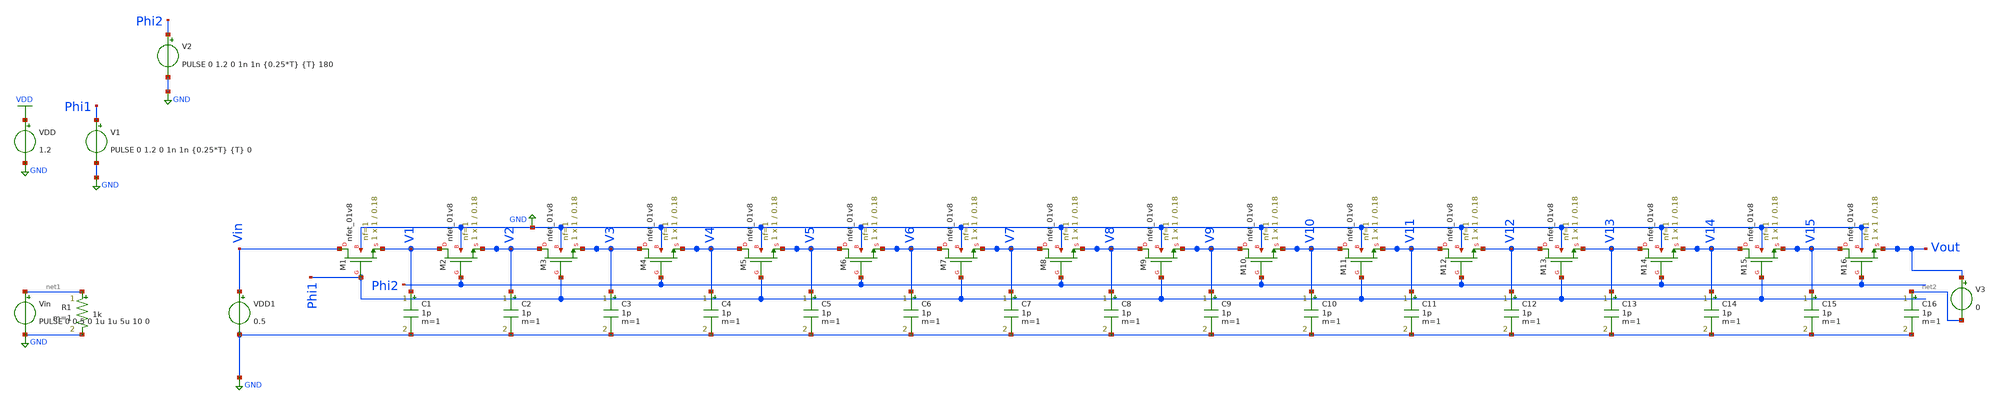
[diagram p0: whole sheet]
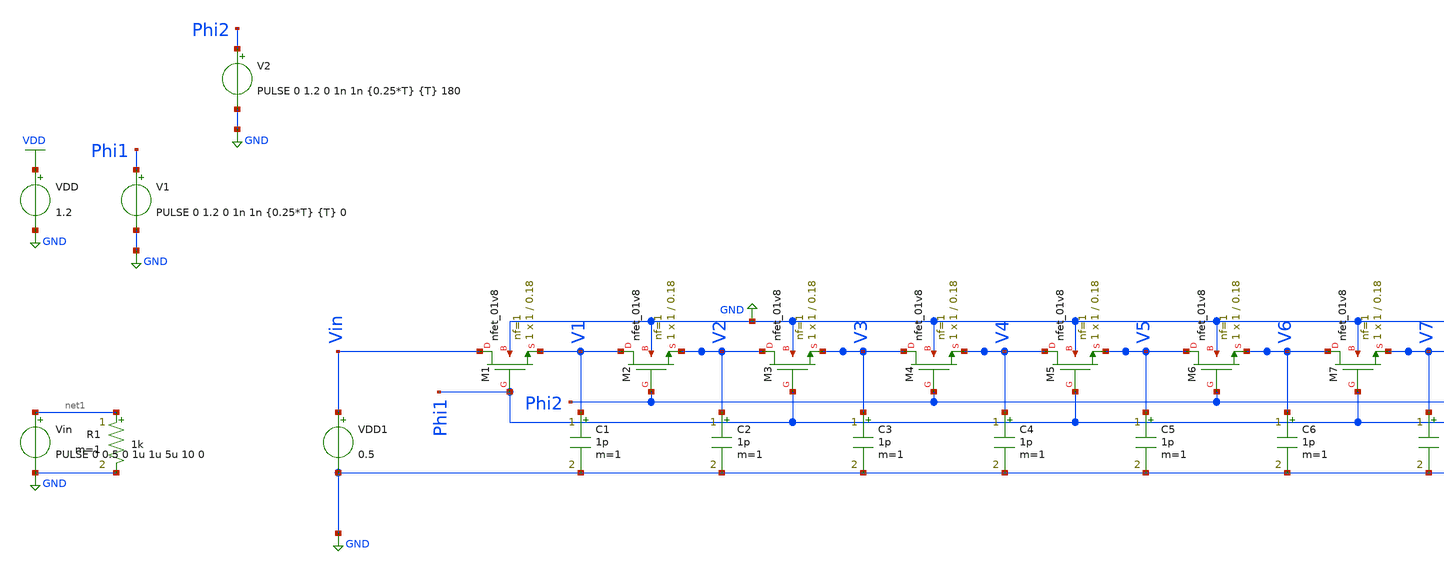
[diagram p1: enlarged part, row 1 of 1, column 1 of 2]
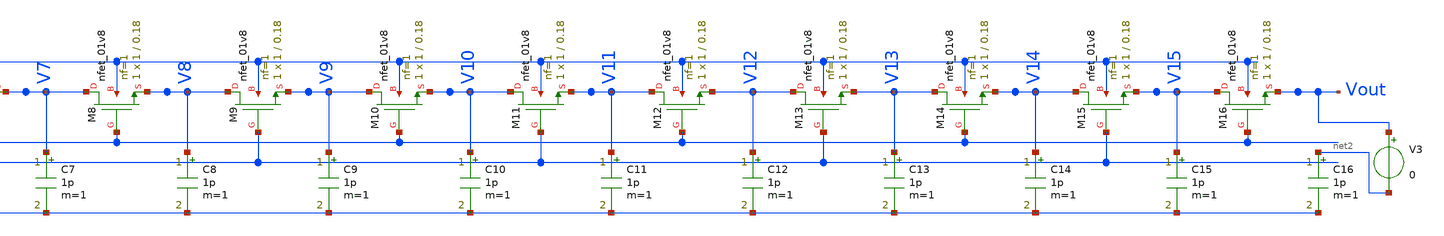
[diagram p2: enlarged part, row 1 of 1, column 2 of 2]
** sch_path: xschem/Switched_Caps/Single_Line_NMOS_Sweep.sch
**.subckt Single_Line_NMOS_Sweep
V1 Phi1 GND PULSE 0 1.2 0 1n 1n {0.25*T} {T} 0
V2 Phi2 GND PULSE 0 1.2 0 1n 1n {0.25*T} {T} 180
Vin net1 GND PULSE 0 0.5 0 1u 1u 5u 10 0
C1 V1 GND 1p m=1
C2 V2 GND 1p m=1
C3 V3 GND 1p m=1
C4 V4 GND 1p m=1
C5 V5 GND 1p m=1
C6 V6 GND 1p m=1
C7 V7 GND 1p m=1
C8 V8 GND 1p m=1
C9 V9 GND 1p m=1
C10 V10 GND 1p m=1
C11 V11 GND 1p m=1
C12 V12 GND 1p m=1
C13 V13 GND 1p m=1
C14 V14 GND 1p m=1
C15 V15 GND 1p m=1
C16 net2 GND 1p m=1
VDD VDD GND 1.2
XM1 Vin Phi1 V1 GND sky130_fd_pr__nfet_01v8 L=0.18 W=1 nf=1 ad='int((nf+1)/2) * W/nf * 0.29' as='int((nf+2)/2) * W/nf * 0.29'
+ pd='2*int((nf+1)/2) * (W/nf + 0.29)' ps='2*int((nf+2)/2) * (W/nf + 0.29)' nrd='0.29 / W' nrs='0.29 / W'
+ sa=0 sb=0 sd=0 mult=1 m=1
XM2 V1 Phi2 V2 GND sky130_fd_pr__nfet_01v8 L=0.18 W=1 nf=1 ad='int((nf+1)/2) * W/nf * 0.29' as='int((nf+2)/2) * W/nf * 0.29'
+ pd='2*int((nf+1)/2) * (W/nf + 0.29)' ps='2*int((nf+2)/2) * (W/nf + 0.29)' nrd='0.29 / W' nrs='0.29 / W'
+ sa=0 sb=0 sd=0 mult=1 m=1
XM3 V2 Phi1 V3 GND sky130_fd_pr__nfet_01v8 L=0.18 W=1 nf=1 ad='int((nf+1)/2) * W/nf * 0.29' as='int((nf+2)/2) * W/nf * 0.29'
+ pd='2*int((nf+1)/2) * (W/nf + 0.29)' ps='2*int((nf+2)/2) * (W/nf + 0.29)' nrd='0.29 / W' nrs='0.29 / W'
+ sa=0 sb=0 sd=0 mult=1 m=1
XM4 V3 Phi2 V4 GND sky130_fd_pr__nfet_01v8 L=0.18 W=1 nf=1 ad='int((nf+1)/2) * W/nf * 0.29' as='int((nf+2)/2) * W/nf * 0.29'
+ pd='2*int((nf+1)/2) * (W/nf + 0.29)' ps='2*int((nf+2)/2) * (W/nf + 0.29)' nrd='0.29 / W' nrs='0.29 / W'
+ sa=0 sb=0 sd=0 mult=1 m=1
XM5 V4 Phi1 V5 GND sky130_fd_pr__nfet_01v8 L=0.18 W=1 nf=1 ad='int((nf+1)/2) * W/nf * 0.29' as='int((nf+2)/2) * W/nf * 0.29'
+ pd='2*int((nf+1)/2) * (W/nf + 0.29)' ps='2*int((nf+2)/2) * (W/nf + 0.29)' nrd='0.29 / W' nrs='0.29 / W'
+ sa=0 sb=0 sd=0 mult=1 m=1
XM6 V5 Phi2 V6 GND sky130_fd_pr__nfet_01v8 L=0.18 W=1 nf=1 ad='int((nf+1)/2) * W/nf * 0.29' as='int((nf+2)/2) * W/nf * 0.29'
+ pd='2*int((nf+1)/2) * (W/nf + 0.29)' ps='2*int((nf+2)/2) * (W/nf + 0.29)' nrd='0.29 / W' nrs='0.29 / W'
+ sa=0 sb=0 sd=0 mult=1 m=1
XM7 V6 Phi1 V7 GND sky130_fd_pr__nfet_01v8 L=0.18 W=1 nf=1 ad='int((nf+1)/2) * W/nf * 0.29' as='int((nf+2)/2) * W/nf * 0.29'
+ pd='2*int((nf+1)/2) * (W/nf + 0.29)' ps='2*int((nf+2)/2) * (W/nf + 0.29)' nrd='0.29 / W' nrs='0.29 / W'
+ sa=0 sb=0 sd=0 mult=1 m=1
XM8 V7 Phi2 V8 GND sky130_fd_pr__nfet_01v8 L=0.18 W=1 nf=1 ad='int((nf+1)/2) * W/nf * 0.29' as='int((nf+2)/2) * W/nf * 0.29'
+ pd='2*int((nf+1)/2) * (W/nf + 0.29)' ps='2*int((nf+2)/2) * (W/nf + 0.29)' nrd='0.29 / W' nrs='0.29 / W'
+ sa=0 sb=0 sd=0 mult=1 m=1
XM9 V8 Phi1 V9 GND sky130_fd_pr__nfet_01v8 L=0.18 W=1 nf=1 ad='int((nf+1)/2) * W/nf * 0.29' as='int((nf+2)/2) * W/nf * 0.29'
+ pd='2*int((nf+1)/2) * (W/nf + 0.29)' ps='2*int((nf+2)/2) * (W/nf + 0.29)' nrd='0.29 / W' nrs='0.29 / W'
+ sa=0 sb=0 sd=0 mult=1 m=1
XM10 V9 Phi2 V10 GND sky130_fd_pr__nfet_01v8 L=0.18 W=1 nf=1 ad='int((nf+1)/2) * W/nf * 0.29' as='int((nf+2)/2) * W/nf * 0.29'
+ pd='2*int((nf+1)/2) * (W/nf + 0.29)' ps='2*int((nf+2)/2) * (W/nf + 0.29)' nrd='0.29 / W' nrs='0.29 / W'
+ sa=0 sb=0 sd=0 mult=1 m=1
XM11 V10 Phi1 V11 GND sky130_fd_pr__nfet_01v8 L=0.18 W=1 nf=1 ad='int((nf+1)/2) * W/nf * 0.29' as='int((nf+2)/2) * W/nf * 0.29'
+ pd='2*int((nf+1)/2) * (W/nf + 0.29)' ps='2*int((nf+2)/2) * (W/nf + 0.29)' nrd='0.29 / W' nrs='0.29 / W'
+ sa=0 sb=0 sd=0 mult=1 m=1
XM12 V11 Phi2 V12 GND sky130_fd_pr__nfet_01v8 L=0.18 W=1 nf=1 ad='int((nf+1)/2) * W/nf * 0.29' as='int((nf+2)/2) * W/nf * 0.29'
+ pd='2*int((nf+1)/2) * (W/nf + 0.29)' ps='2*int((nf+2)/2) * (W/nf + 0.29)' nrd='0.29 / W' nrs='0.29 / W'
+ sa=0 sb=0 sd=0 mult=1 m=1
XM13 V12 Phi1 V13 GND sky130_fd_pr__nfet_01v8 L=0.18 W=1 nf=1 ad='int((nf+1)/2) * W/nf * 0.29' as='int((nf+2)/2) * W/nf * 0.29'
+ pd='2*int((nf+1)/2) * (W/nf + 0.29)' ps='2*int((nf+2)/2) * (W/nf + 0.29)' nrd='0.29 / W' nrs='0.29 / W'
+ sa=0 sb=0 sd=0 mult=1 m=1
XM14 V13 Phi2 V14 GND sky130_fd_pr__nfet_01v8 L=0.18 W=1 nf=1 ad='int((nf+1)/2) * W/nf * 0.29' as='int((nf+2)/2) * W/nf * 0.29'
+ pd='2*int((nf+1)/2) * (W/nf + 0.29)' ps='2*int((nf+2)/2) * (W/nf + 0.29)' nrd='0.29 / W' nrs='0.29 / W'
+ sa=0 sb=0 sd=0 mult=1 m=1
XM15 V14 Phi1 V15 GND sky130_fd_pr__nfet_01v8 L=0.18 W=1 nf=1 ad='int((nf+1)/2) * W/nf * 0.29' as='int((nf+2)/2) * W/nf * 0.29'
+ pd='2*int((nf+1)/2) * (W/nf + 0.29)' ps='2*int((nf+2)/2) * (W/nf + 0.29)' nrd='0.29 / W' nrs='0.29 / W'
+ sa=0 sb=0 sd=0 mult=1 m=1
XM16 V15 Phi2 Vout GND sky130_fd_pr__nfet_01v8 L=0.18 W=1 nf=1 ad='int((nf+1)/2) * W/nf * 0.29' as='int((nf+2)/2) * W/nf * 0.29'
+ pd='2*int((nf+1)/2) * (W/nf + 0.29)' ps='2*int((nf+2)/2) * (W/nf + 0.29)' nrd='0.29 / W' nrs='0.29 / W'
+ sa=0 sb=0 sd=0 mult=1 m=1
VDD1 Vin GND 0.5
R1 net1 GND 1k m=1
V3 Vout net2 0
**** begin user architecture code


.lib /home/sky/sky130A/libs.tech/ngspice/sky130.lib.spice tt
.options abstol=1e-14 reltol=1e-4
.param T=1u
*.tran 10u 2m

* from https://sourceforge.net/p/ngspice/ngspice/ci/master/tree/examples/Monte_Carlo/MonteCarlo.sp

.control
let T_start = 4u
let T_stop = 12u
let T_step = 4u
let T_act = T_start

let run = 0
set curplot=new          $ create a new plot
set scratch=$curplot     $ store its name to 'scratch'
setplot $scratch         $ make 'scratch' the active plot

* loop
while T_act le T_stop
  alterparam T=T_act
  tran 0.5u 6m

  set run = $&run             $ create a variable from the vector
  set dt = $curplot           $ store the current plot to dt
  setplot $scratch            $ make 'scratch' the active plot
  let vout{$run}={$dt}.v(Vout) $ store the output vector to plot 'scratch'
  setplot $dt                 $ go back to the previous plot
  let run = run + 1
  let T_act = T_act + T_step
end

plot {$scratch}.allv

.endc
.save all


**** end user architecture code
**.ends
.GLOBAL GND
.GLOBAL VDD
.end
